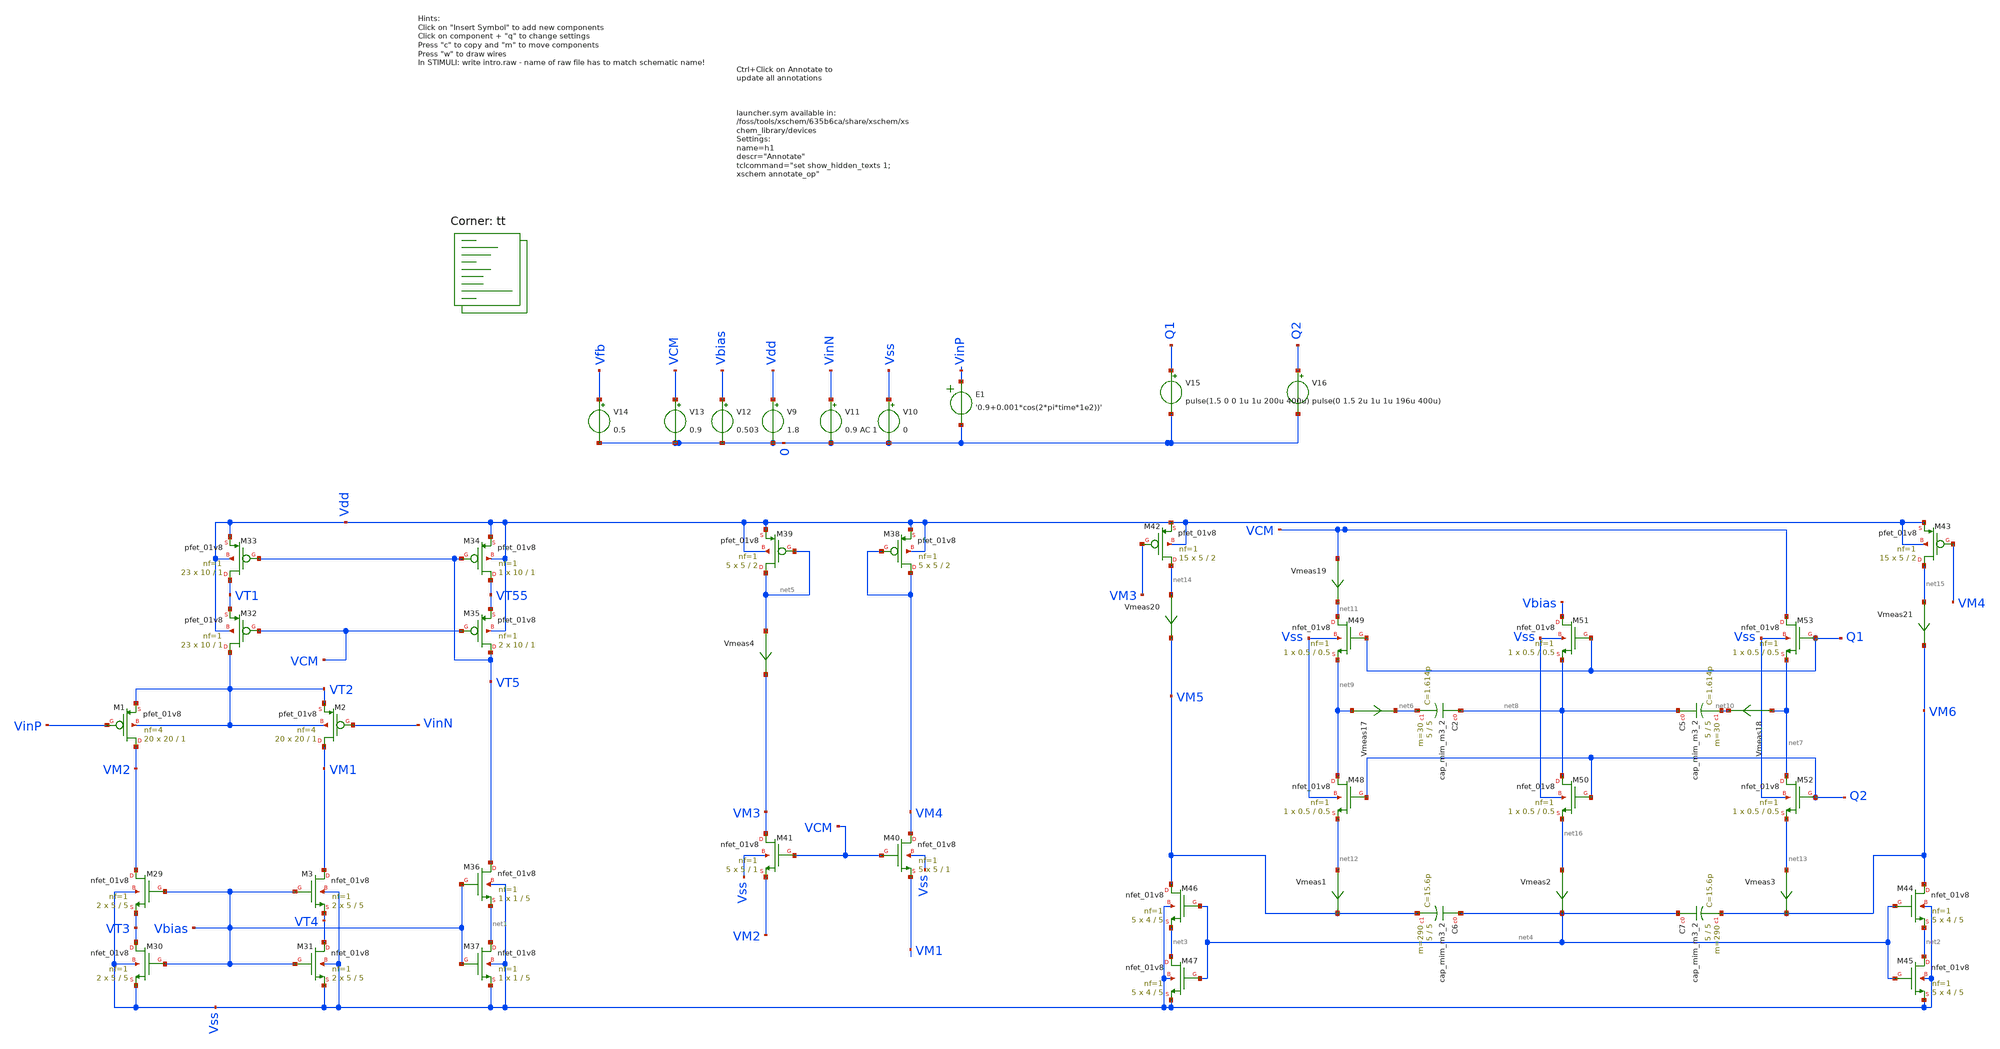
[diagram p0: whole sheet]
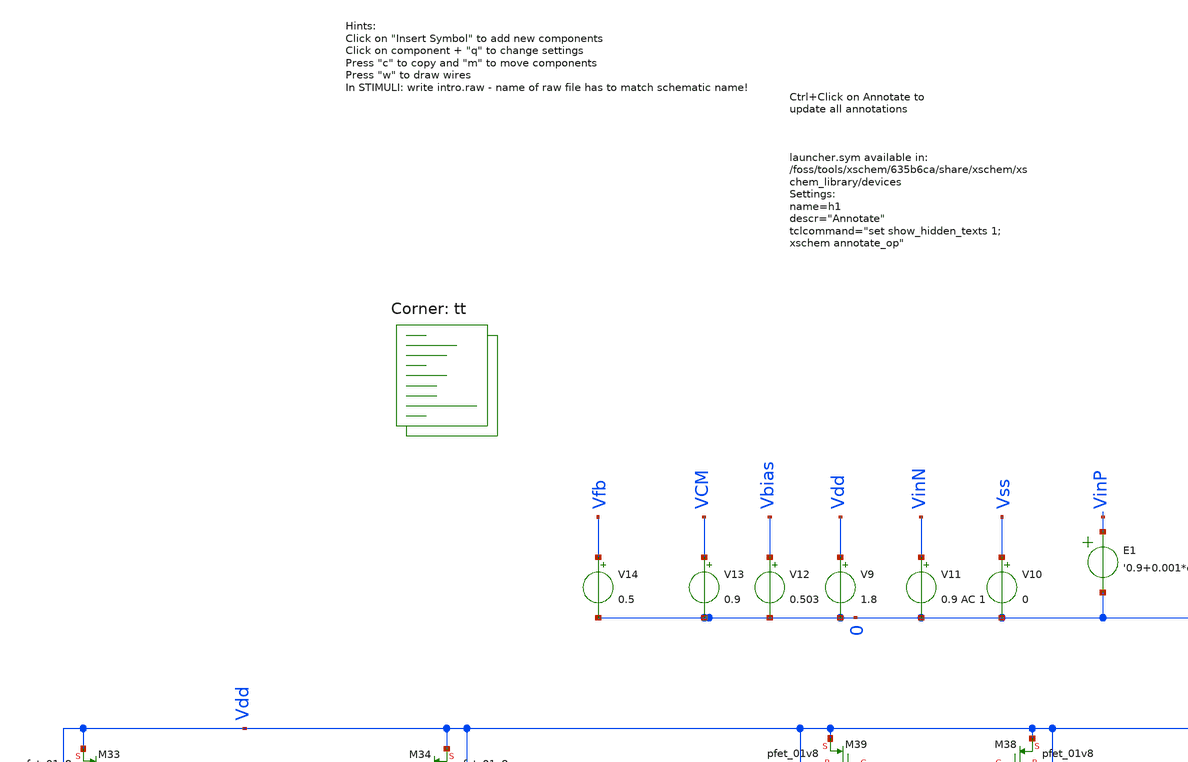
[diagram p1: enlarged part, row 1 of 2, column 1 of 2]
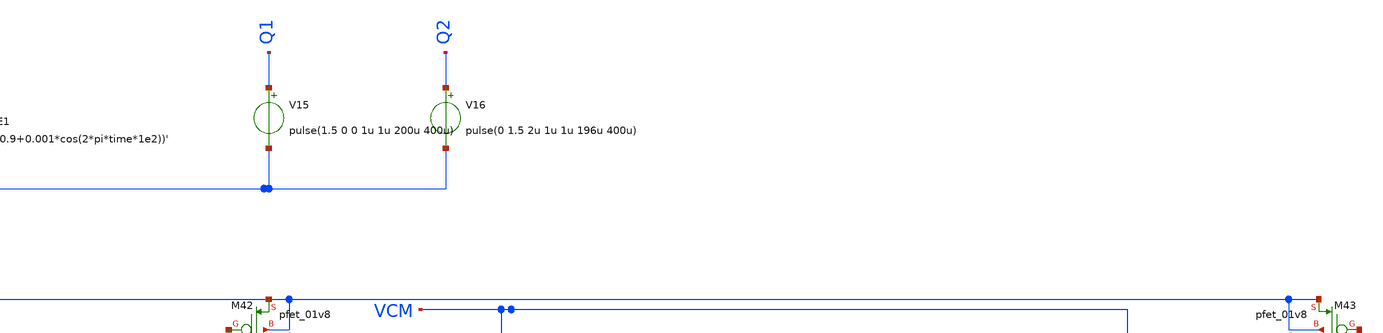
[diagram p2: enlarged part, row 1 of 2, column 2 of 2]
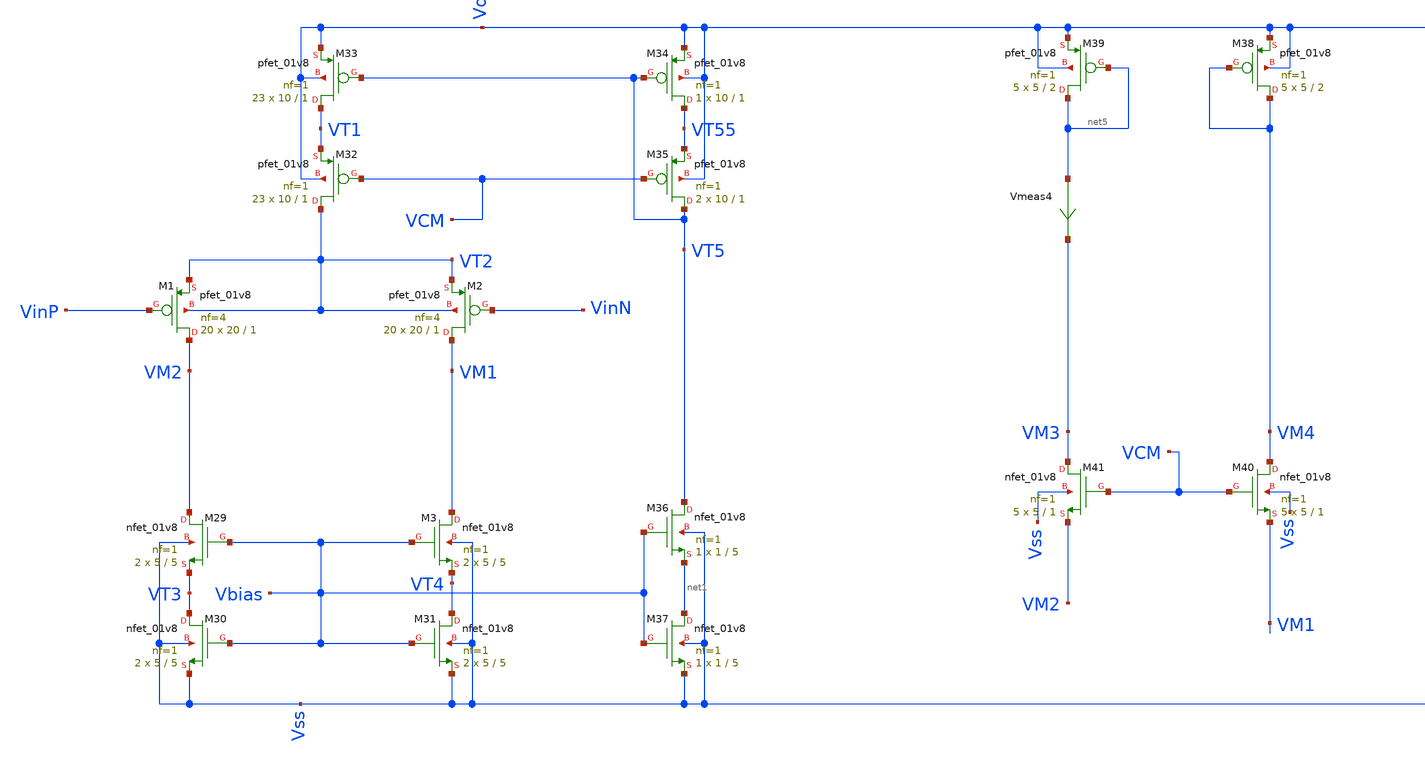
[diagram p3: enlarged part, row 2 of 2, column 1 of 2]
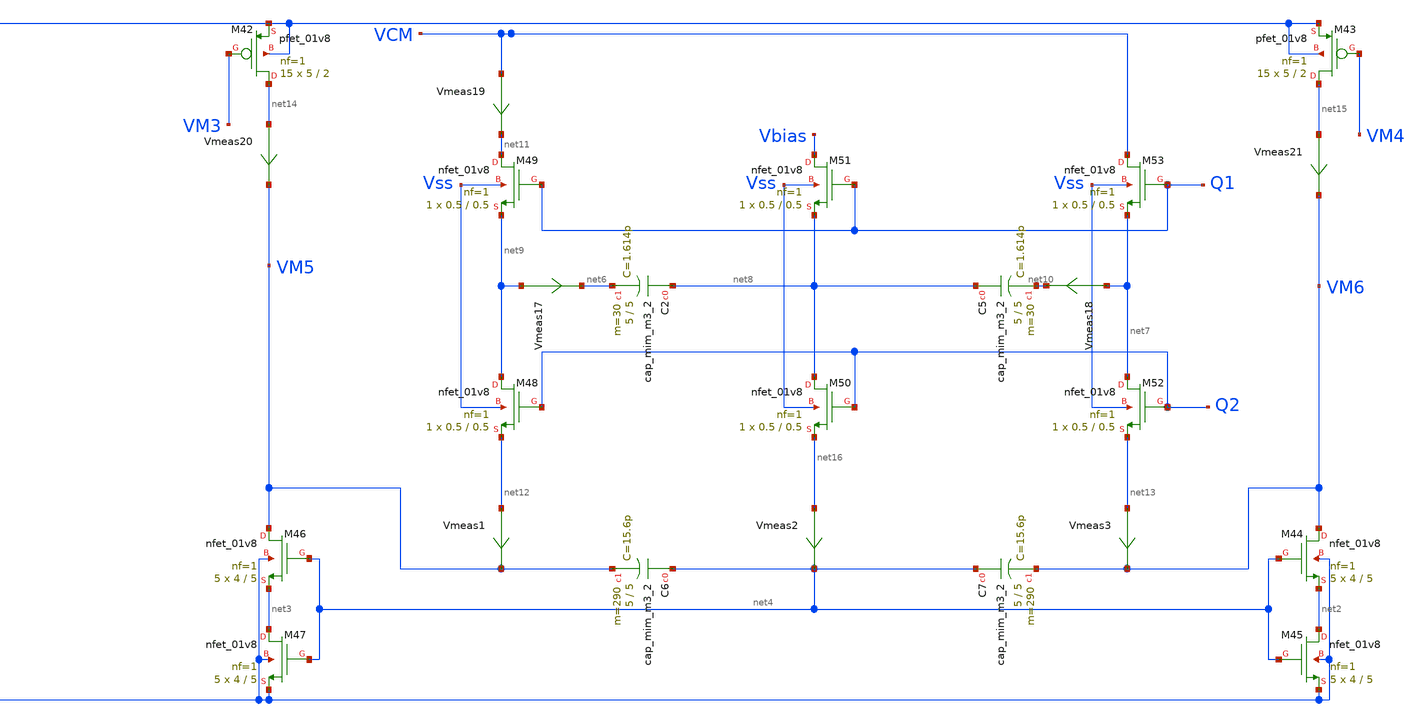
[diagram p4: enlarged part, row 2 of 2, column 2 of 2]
** sch_path: Backup16-01.sch
**.subckt Backup16-01
XM1 VM2 VinP VT2 VT2 sky130_fd_pr__pfet_01v8 L=1 W=20 nf=4 ad='int((nf+1)/2) * W/nf * 0.29' as='int((nf+2)/2) * W/nf * 0.29'
+ pd='2*int((nf+1)/2) * (W/nf + 0.29)' ps='2*int((nf+2)/2) * (W/nf + 0.29)' nrd='0.29 / W' nrs='0.29 / W'
+ sa=0 sb=0 sd=0 mult=20 m=20
XM2 VM1 VinN VT2 VT2 sky130_fd_pr__pfet_01v8 L=1 W=20 nf=4 ad='int((nf+1)/2) * W/nf * 0.29' as='int((nf+2)/2) * W/nf * 0.29'
+ pd='2*int((nf+1)/2) * (W/nf + 0.29)' ps='2*int((nf+2)/2) * (W/nf + 0.29)' nrd='0.29 / W' nrs='0.29 / W'
+ sa=0 sb=0 sd=0 mult=20 m=20
XM3 VM1 Vbias VT4 Vss sky130_fd_pr__nfet_01v8 L=5 W=5 nf=1 ad='int((nf+1)/2) * W/nf * 0.29' as='int((nf+2)/2) * W/nf * 0.29'
+ pd='2*int((nf+1)/2) * (W/nf + 0.29)' ps='2*int((nf+2)/2) * (W/nf + 0.29)' nrd='0.29 / W' nrs='0.29 / W'
+ sa=0 sb=0 sd=0 mult=2 m=2
XM29 VM2 Vbias VT3 Vss sky130_fd_pr__nfet_01v8 L=5 W=5 nf=1 ad='int((nf+1)/2) * W/nf * 0.29' as='int((nf+2)/2) * W/nf * 0.29'
+ pd='2*int((nf+1)/2) * (W/nf + 0.29)' ps='2*int((nf+2)/2) * (W/nf + 0.29)' nrd='0.29 / W' nrs='0.29 / W'
+ sa=0 sb=0 sd=0 mult=2 m=2
XM30 VT3 Vbias Vss Vss sky130_fd_pr__nfet_01v8 L=5 W=5 nf=1 ad='int((nf+1)/2) * W/nf * 0.29' as='int((nf+2)/2) * W/nf * 0.29'
+ pd='2*int((nf+1)/2) * (W/nf + 0.29)' ps='2*int((nf+2)/2) * (W/nf + 0.29)' nrd='0.29 / W' nrs='0.29 / W'
+ sa=0 sb=0 sd=0 mult=2 m=2
XM31 VT4 Vbias Vss Vss sky130_fd_pr__nfet_01v8 L=5 W=5 nf=1 ad='int((nf+1)/2) * W/nf * 0.29' as='int((nf+2)/2) * W/nf * 0.29'
+ pd='2*int((nf+1)/2) * (W/nf + 0.29)' ps='2*int((nf+2)/2) * (W/nf + 0.29)' nrd='0.29 / W' nrs='0.29 / W'
+ sa=0 sb=0 sd=0 mult=2 m=2
XM32 VT2 VCM VT1 Vdd sky130_fd_pr__pfet_01v8 L=1 W=10 nf=1 ad='int((nf+1)/2) * W/nf * 0.29' as='int((nf+2)/2) * W/nf * 0.29'
+ pd='2*int((nf+1)/2) * (W/nf + 0.29)' ps='2*int((nf+2)/2) * (W/nf + 0.29)' nrd='0.29 / W' nrs='0.29 / W'
+ sa=0 sb=0 sd=0 mult=23 m=23
XM33 VT1 VT5 Vdd Vdd sky130_fd_pr__pfet_01v8 L=1 W=10 nf=1 ad='int((nf+1)/2) * W/nf * 0.29' as='int((nf+2)/2) * W/nf * 0.29'
+ pd='2*int((nf+1)/2) * (W/nf + 0.29)' ps='2*int((nf+2)/2) * (W/nf + 0.29)' nrd='0.29 / W' nrs='0.29 / W'
+ sa=0 sb=0 sd=0 mult=23 m=23
XM34 VT55 VT5 Vdd Vdd sky130_fd_pr__pfet_01v8 L=1 W=10 nf=1 ad='int((nf+1)/2) * W/nf * 0.29' as='int((nf+2)/2) * W/nf * 0.29'
+ pd='2*int((nf+1)/2) * (W/nf + 0.29)' ps='2*int((nf+2)/2) * (W/nf + 0.29)' nrd='0.29 / W' nrs='0.29 / W'
+ sa=0 sb=0 sd=0 mult=1 m=1
XM35 VT5 VCM VT55 Vdd sky130_fd_pr__pfet_01v8 L=1 W=10 nf=1 ad='int((nf+1)/2) * W/nf * 0.29' as='int((nf+2)/2) * W/nf * 0.29'
+ pd='2*int((nf+1)/2) * (W/nf + 0.29)' ps='2*int((nf+2)/2) * (W/nf + 0.29)' nrd='0.29 / W' nrs='0.29 / W'
+ sa=0 sb=0 sd=0 mult=2 m=2
XM36 VT5 Vbias net1 Vss sky130_fd_pr__nfet_01v8 L=5 W=1 nf=1 ad='int((nf+1)/2) * W/nf * 0.29' as='int((nf+2)/2) * W/nf * 0.29'
+ pd='2*int((nf+1)/2) * (W/nf + 0.29)' ps='2*int((nf+2)/2) * (W/nf + 0.29)' nrd='0.29 / W' nrs='0.29 / W'
+ sa=0 sb=0 sd=0 mult=1 m=1
XM37 net1 Vbias Vss Vss sky130_fd_pr__nfet_01v8 L=5 W=1 nf=1 ad='int((nf+1)/2) * W/nf * 0.29' as='int((nf+2)/2) * W/nf * 0.29'
+ pd='2*int((nf+1)/2) * (W/nf + 0.29)' ps='2*int((nf+2)/2) * (W/nf + 0.29)' nrd='0.29 / W' nrs='0.29 / W'
+ sa=0 sb=0 sd=0 mult=1 m=1
XM38 VM4 VM4 Vdd Vdd sky130_fd_pr__pfet_01v8 L=2 W=5 nf=1 ad='int((nf+1)/2) * W/nf * 0.29' as='int((nf+2)/2) * W/nf * 0.29'
+ pd='2*int((nf+1)/2) * (W/nf + 0.29)' ps='2*int((nf+2)/2) * (W/nf + 0.29)' nrd='0.29 / W' nrs='0.29 / W'
+ sa=0 sb=0 sd=0 mult=5 m=5
XM39 net5 net5 Vdd Vdd sky130_fd_pr__pfet_01v8 L=2 W=5 nf=1 ad='int((nf+1)/2) * W/nf * 0.29' as='int((nf+2)/2) * W/nf * 0.29'
+ pd='2*int((nf+1)/2) * (W/nf + 0.29)' ps='2*int((nf+2)/2) * (W/nf + 0.29)' nrd='0.29 / W' nrs='0.29 / W'
+ sa=0 sb=0 sd=0 mult=5 m=5
XM40 VM4 VCM VM1 Vss sky130_fd_pr__nfet_01v8 L=1 W=5 nf=1 ad='int((nf+1)/2) * W/nf * 0.29' as='int((nf+2)/2) * W/nf * 0.29'
+ pd='2*int((nf+1)/2) * (W/nf + 0.29)' ps='2*int((nf+2)/2) * (W/nf + 0.29)' nrd='0.29 / W' nrs='0.29 / W'
+ sa=0 sb=0 sd=0 mult=5 m=5
XM41 VM3 VCM VM2 Vss sky130_fd_pr__nfet_01v8 L=1 W=5 nf=1 ad='int((nf+1)/2) * W/nf * 0.29' as='int((nf+2)/2) * W/nf * 0.29'
+ pd='2*int((nf+1)/2) * (W/nf + 0.29)' ps='2*int((nf+2)/2) * (W/nf + 0.29)' nrd='0.29 / W' nrs='0.29 / W'
+ sa=0 sb=0 sd=0 mult=5 m=5
XM42 net14 VM3 Vdd Vdd sky130_fd_pr__pfet_01v8 L=2 W=5 nf=1 ad='int((nf+1)/2) * W/nf * 0.29' as='int((nf+2)/2) * W/nf * 0.29'
+ pd='2*int((nf+1)/2) * (W/nf + 0.29)' ps='2*int((nf+2)/2) * (W/nf + 0.29)' nrd='0.29 / W' nrs='0.29 / W'
+ sa=0 sb=0 sd=0 mult=15 m=15
XM43 net15 VM4 Vdd Vdd sky130_fd_pr__pfet_01v8 L=2 W=5 nf=1 ad='int((nf+1)/2) * W/nf * 0.29' as='int((nf+2)/2) * W/nf * 0.29'
+ pd='2*int((nf+1)/2) * (W/nf + 0.29)' ps='2*int((nf+2)/2) * (W/nf + 0.29)' nrd='0.29 / W' nrs='0.29 / W'
+ sa=0 sb=0 sd=0 mult=15 m=15
XM44 VM6 net4 net2 Vss sky130_fd_pr__nfet_01v8 L=5 W=4 nf=1 ad='int((nf+1)/2) * W/nf * 0.29' as='int((nf+2)/2) * W/nf * 0.29'
+ pd='2*int((nf+1)/2) * (W/nf + 0.29)' ps='2*int((nf+2)/2) * (W/nf + 0.29)' nrd='0.29 / W' nrs='0.29 / W'
+ sa=0 sb=0 sd=0 mult=5 m=5
XM45 net2 net4 Vss Vss sky130_fd_pr__nfet_01v8 L=5 W=4 nf=1 ad='int((nf+1)/2) * W/nf * 0.29' as='int((nf+2)/2) * W/nf * 0.29'
+ pd='2*int((nf+1)/2) * (W/nf + 0.29)' ps='2*int((nf+2)/2) * (W/nf + 0.29)' nrd='0.29 / W' nrs='0.29 / W'
+ sa=0 sb=0 sd=0 mult=5 m=5
XM46 VM5 net4 net3 Vss sky130_fd_pr__nfet_01v8 L=5 W=4 nf=1 ad='int((nf+1)/2) * W/nf * 0.29' as='int((nf+2)/2) * W/nf * 0.29'
+ pd='2*int((nf+1)/2) * (W/nf + 0.29)' ps='2*int((nf+2)/2) * (W/nf + 0.29)' nrd='0.29 / W' nrs='0.29 / W'
+ sa=0 sb=0 sd=0 mult=5 m=5
XM47 net3 net4 Vss Vss sky130_fd_pr__nfet_01v8 L=5 W=4 nf=1 ad='int((nf+1)/2) * W/nf * 0.29' as='int((nf+2)/2) * W/nf * 0.29'
+ pd='2*int((nf+1)/2) * (W/nf + 0.29)' ps='2*int((nf+2)/2) * (W/nf + 0.29)' nrd='0.29 / W' nrs='0.29 / W'
+ sa=0 sb=0 sd=0 mult=5 m=5
E1 VinP 0 VOL=' '0.9+0.001*cos(2*pi*time*1e2))' '
V9 Vdd 0 1.8
V10 Vss 0 0
V11 VinN 0 0.9 AC 1
V12 Vbias 0 0.503
V13 VCM 0 0.9
V14 Vfb 0 0.5
XC2 net8 net6 sky130_fd_pr__cap_mim_m3_2 W=5 L=5 MF=30 m=30
XC5 net8 net10 sky130_fd_pr__cap_mim_m3_2 W=5 L=5 MF=30 m=30
XC6 net4 VM5 sky130_fd_pr__cap_mim_m3_2 W=5 L=5 MF=290 m=290
XC7 net4 VM6 sky130_fd_pr__cap_mim_m3_2 W=5 L=5 MF=290 m=290
XM48 net9 Q2 net12 Vss sky130_fd_pr__nfet_01v8 L=0.5 W=0.5 nf=1 ad='int((nf+1)/2) * W/nf * 0.29' as='int((nf+2)/2) * W/nf * 0.29'
+ pd='2*int((nf+1)/2) * (W/nf + 0.29)' ps='2*int((nf+2)/2) * (W/nf + 0.29)' nrd='0.29 / W' nrs='0.29 / W'
+ sa=0 sb=0 sd=0 mult=1 m=1
XM49 net11 Q1 net9 Vss sky130_fd_pr__nfet_01v8 L=0.5 W=0.5 nf=1 ad='int((nf+1)/2) * W/nf * 0.29' as='int((nf+2)/2) * W/nf * 0.29'
+ pd='2*int((nf+1)/2) * (W/nf + 0.29)' ps='2*int((nf+2)/2) * (W/nf + 0.29)' nrd='0.29 / W' nrs='0.29 / W'
+ sa=0 sb=0 sd=0 mult=1 m=1
XM50 net8 Q2 net16 Vss sky130_fd_pr__nfet_01v8 L=0.5 W=0.5 nf=1 ad='int((nf+1)/2) * W/nf * 0.29' as='int((nf+2)/2) * W/nf * 0.29'
+ pd='2*int((nf+1)/2) * (W/nf + 0.29)' ps='2*int((nf+2)/2) * (W/nf + 0.29)' nrd='0.29 / W' nrs='0.29 / W'
+ sa=0 sb=0 sd=0 mult=1 m=1
XM51 Vbias Q1 net8 Vss sky130_fd_pr__nfet_01v8 L=0.5 W=0.5 nf=1 ad='int((nf+1)/2) * W/nf * 0.29' as='int((nf+2)/2) * W/nf * 0.29'
+ pd='2*int((nf+1)/2) * (W/nf + 0.29)' ps='2*int((nf+2)/2) * (W/nf + 0.29)' nrd='0.29 / W' nrs='0.29 / W'
+ sa=0 sb=0 sd=0 mult=1 m=1
XM52 net7 Q2 net13 Vss sky130_fd_pr__nfet_01v8 L=0.5 W=0.5 nf=1 ad='int((nf+1)/2) * W/nf * 0.29' as='int((nf+2)/2) * W/nf * 0.29'
+ pd='2*int((nf+1)/2) * (W/nf + 0.29)' ps='2*int((nf+2)/2) * (W/nf + 0.29)' nrd='0.29 / W' nrs='0.29 / W'
+ sa=0 sb=0 sd=0 mult=1 m=1
XM53 VCM Q1 net7 Vss sky130_fd_pr__nfet_01v8 L=0.5 W=0.5 nf=1 ad='int((nf+1)/2) * W/nf * 0.29' as='int((nf+2)/2) * W/nf * 0.29'
+ pd='2*int((nf+1)/2) * (W/nf + 0.29)' ps='2*int((nf+2)/2) * (W/nf + 0.29)' nrd='0.29 / W' nrs='0.29 / W'
+ sa=0 sb=0 sd=0 mult=1 m=1
V15 Q1 0 pulse(1.5 0 0 1u 1u 200u 400u)
V16 Q2 0 pulse(0 1.5 2u 1u 1u 196u 400u)
Vmeas17 net9 net6 0
.save i(vmeas17)
Vmeas18 net7 net10 0
.save i(vmeas18)
Vmeas19 VCM net11 0
.save i(vmeas19)
Vmeas20 net14 VM5 0
.save i(vmeas20)
Vmeas21 net15 VM6 0
.save i(vmeas21)
Vmeas1 net12 VM5 0
.save i(vmeas1)
Vmeas2 net16 net4 0
.save i(vmeas2)
Vmeas3 net13 VM6 0
.save i(vmeas3)
Vmeas4 net5 VM3 0
.save i(vmeas4)
**** begin user architecture code


.options savecurrents
.control



save all
save @m.xm1.msky130_fd_pr__nfet_01v8_lvt[id]
save @m.xm1.msky130_fd_pr__pfet_01v8[id]
save @m.xm7.msky130_fd_pr__pfet_01v8[id]
save @m.xm1.msky130_fd_pr__nfet_01v8_lvt[vth]
save @m.xm11.msky130_fd_pr__pfet_01v8[vth]
save @m.xm1.msky130_fd_pr__nfet_01v8_lvt[vgs]
save @m.xm1.msky130_fd_pr__nfet_01v8_lvt[vds]
save @m.xm1.msky130_fd_pr__nfet_01v8_lvt[gm]
save @m.xm1.msky130_fd_pr__nfet_01v8_lvt[gds]
save @m.xm23.msky130_fd_pr__nfet_01v8[cgs]
save @m.xm15.msky130_fd_pr__nfet_01v8[cgs]

save @m.xm1.msky130_fd_pr__pfet_01v8[id]
save @m.xm2.msky130_fd_pr__pfet_01v8_lvt[id]
save @m.xm2.msky130_fd_pr__pfet_01v8_lvt[vth]
save @m.xm1.msky130_fd_pr__pfet_01v8[vgs]
save @m.xm2.msky130_fd_pr__pfet_01v8_lvt[vds]
save @m.xm2.msky130_fd_pr__pfet_01v8_lvt[gm]
save @m.xm2.msky130_fd_pr__pfet_01v8_lvt[gds]
save @m.xm2.msky130_fd_pr__pfet_01v8_lvt[cgs]

op
remzerovec
write intro.raw
*set appendwrite

*dc V1 0 1.8 0.01
*plot @m.xm1.msky130_fd_pr__nfet_01v8_lvt[id] @m.xm2.msky130_fd_pr__pfet_01v8_lvt[id]
*remzerovec
*write intro.raw

.endc
.control
tran 500u 0.75
save all
plot v(VM5)
plot v(VM6)-v(VM5)

noise V(VM5,VM6) V11 dec 100 0.1 100
print inoise_total onoise_total
setplot noise1
plot inoise_spectrum


.endc





.lib $::SKYWATER_MODELS/sky130.lib.spice tt
**** end user architecture code
**.ends
.end
